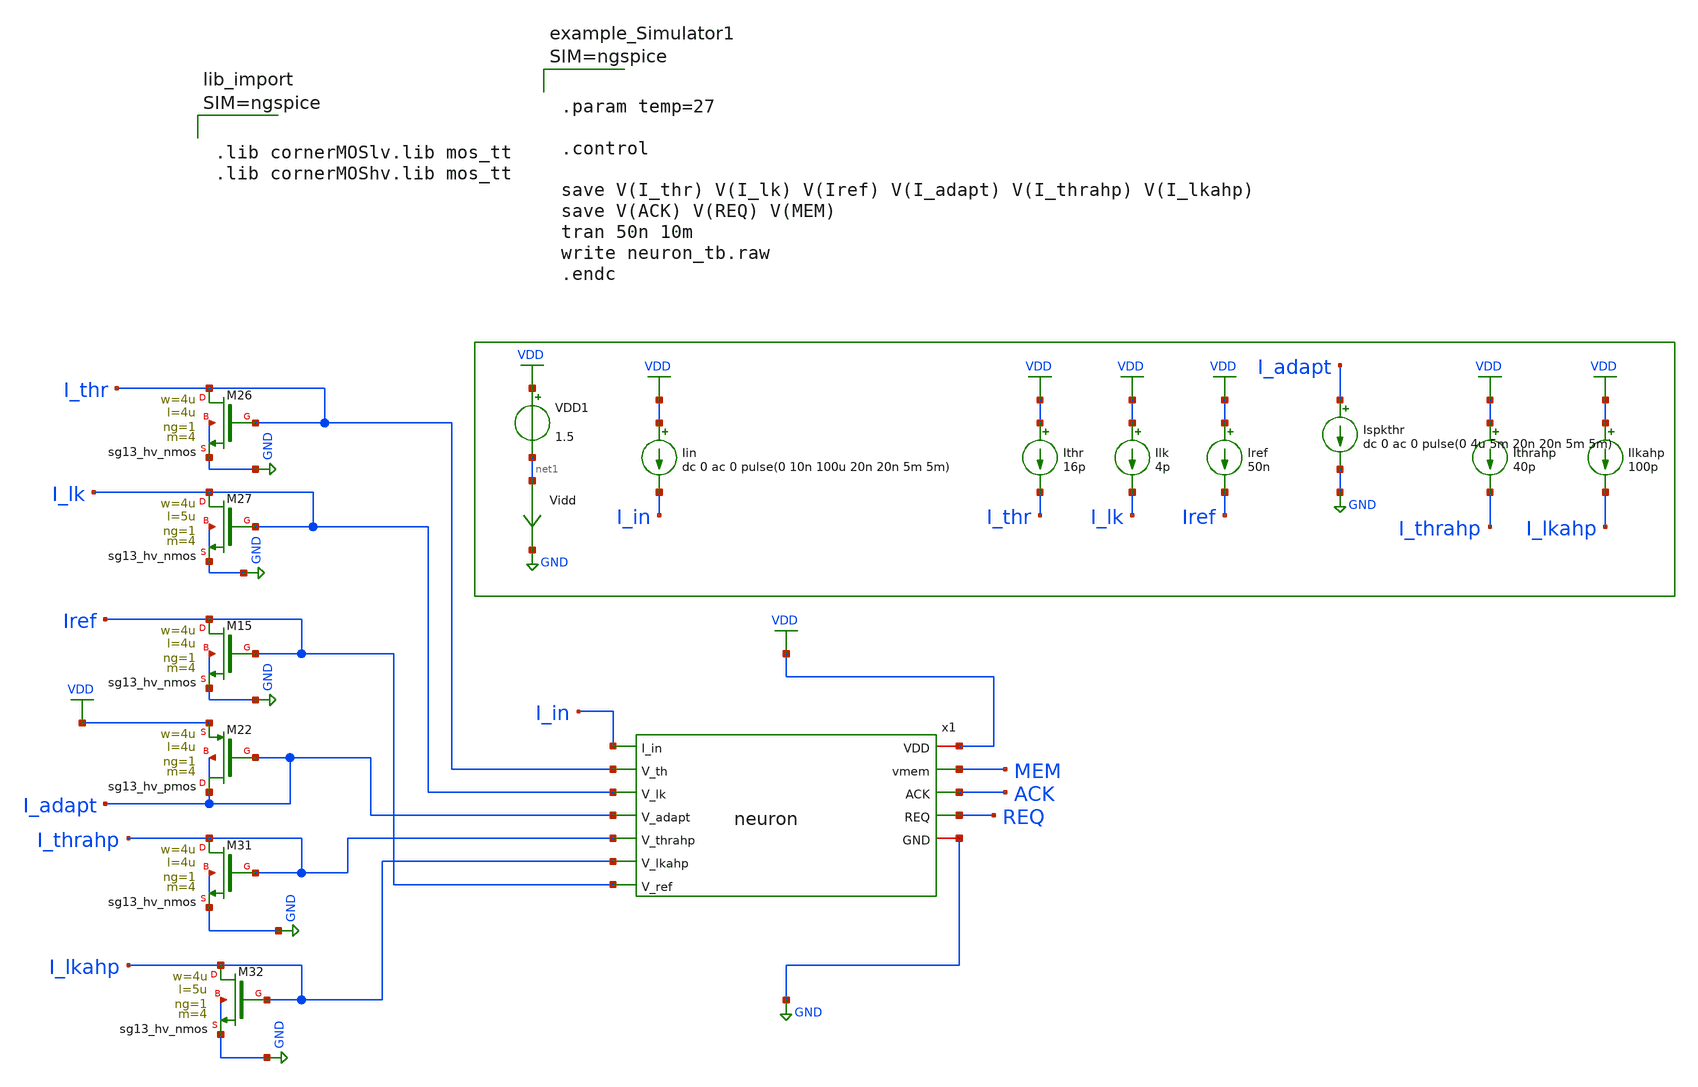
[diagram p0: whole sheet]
** sch_path: xschem/neuron_tb.sch
**.subckt neuron_tb
x1 VDD I_in I_thr I_lk MEM ACK REQ I_adapt I_thrahp I_lkahp Iref GND neuron
Ithr VDD I_thr 16p
Ilk VDD I_lk 4p
Ispkthr I_adapt GND dc 0 ac 0 pulse(0 4u 5m 20n 20n 5m 5m)
Iin VDD I_in dc 0 ac 0 pulse(0 10n 100u 20n 20n 5m 5m)
VDD1 VDD net1 1.5
Iref VDD Iref 50n
Vidd net1 GND 0
.save i(vidd)
Ilkahp VDD I_lkahp 100p
Ithrahp VDD I_thrahp 40p
XM26 I_thr I_thr GND GND sg13_hv_nmos w=4u l=4u ng=1 m=4 mm_ok=1
XM27 I_lk I_lk GND GND sg13_hv_nmos w=4u l=5u ng=1 m=4 mm_ok=1
XM15 Iref Iref GND GND sg13_hv_nmos w=4u l=4u ng=1 m=4 mm_ok=1
XM22 I_adapt I_adapt VDD I_adapt sg13_hv_pmos w=4u l=4u ng=1 m=4 mm_ok=1
XM31 I_thrahp I_thrahp GND GND sg13_hv_nmos w=4u l=4u ng=1 m=4 mm_ok=1
XM32 I_lkahp I_lkahp GND GND sg13_hv_nmos w=4u l=5u ng=1 m=4 mm_ok=1
**** begin user architecture code



.param temp=27

.control

save V(I_thr) V(I_lk) V(Iref) V(I_adapt) V(I_thrahp) V(I_lkahp)
save V(ACK) V(REQ) V(MEM)
tran 50n 10m
write neuron_tb.raw
.endc







.lib cornerMOSlv.lib mos_tt
.lib cornerMOShv.lib mos_tt


**** end user architecture code
**.ends
.GLOBAL GND
.GLOBAL VDD
.end
